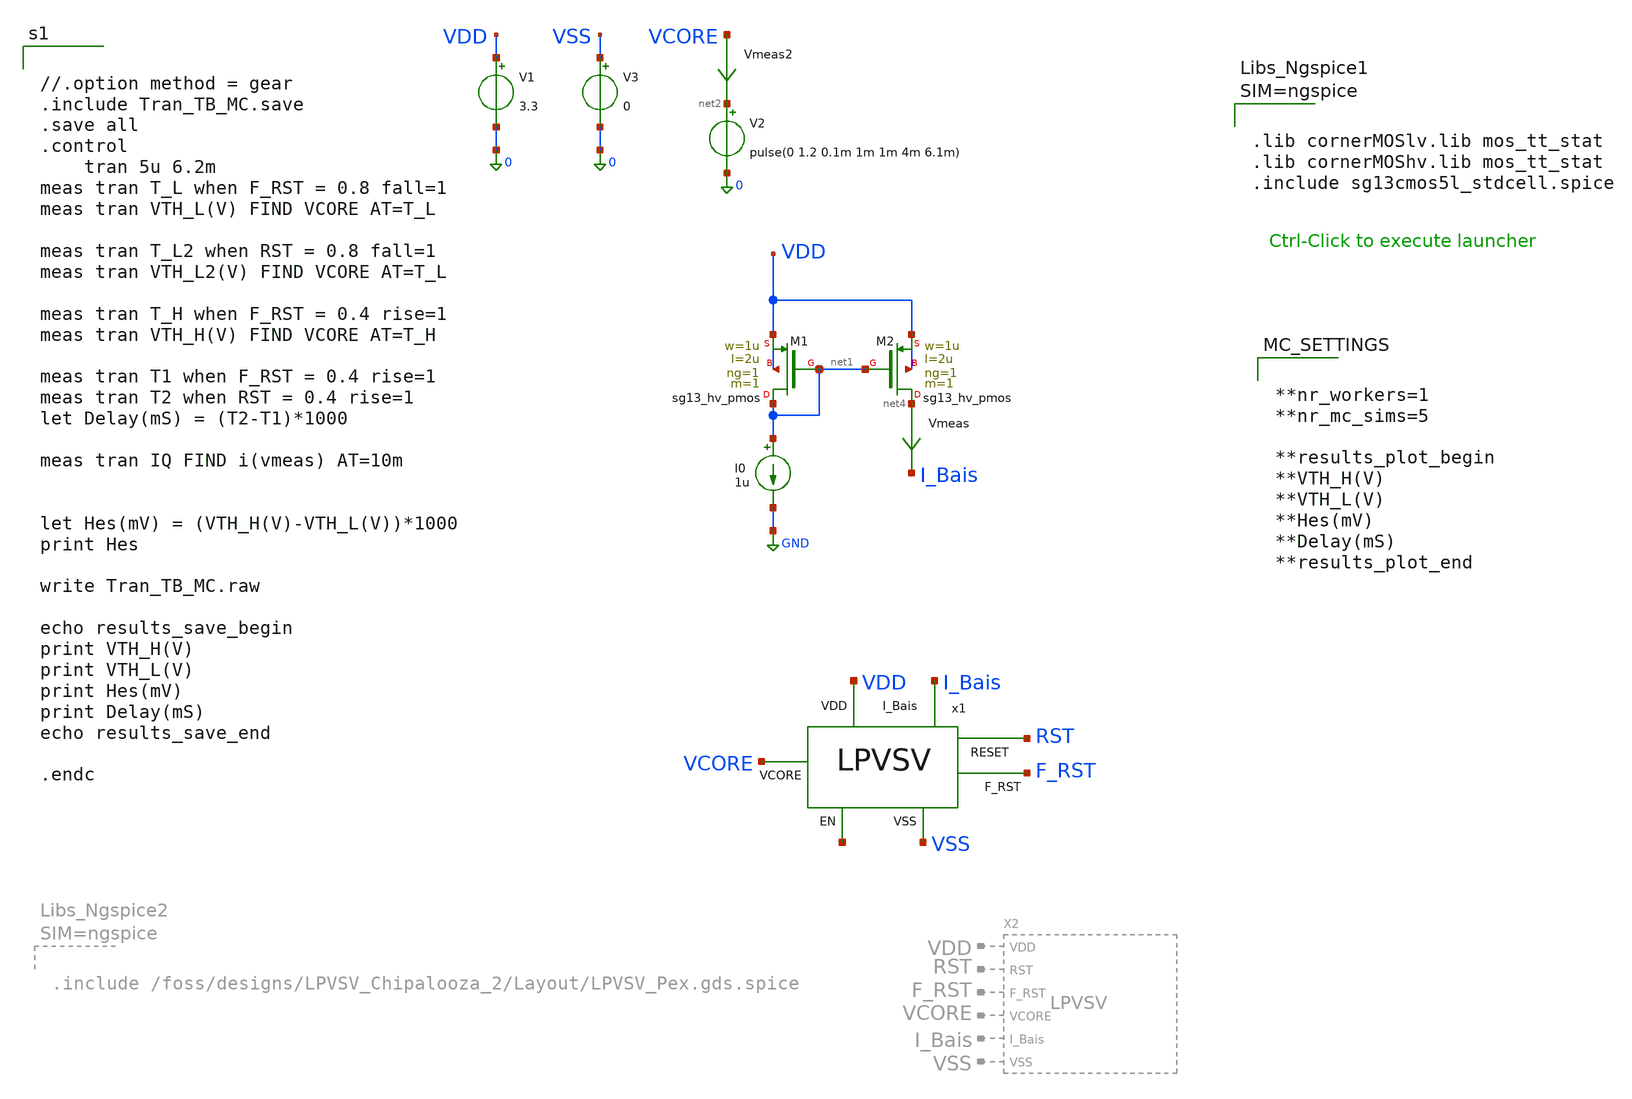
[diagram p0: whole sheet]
** sch_path: Simulation/Tran_TB_MC.sch
**.subckt Tran_TB_MC
V1 VDD 0 3.3
V2 net2 0 pulse(0 1.2 0.1m 1m 1m 4m 6.1m)
Vmeas2 VCORE net2 0
.save i(vmeas2)
V3 VSS 0 0
x1 VDD VCORE I_Bais RST F_RST VSS net3 LPVSV
I0 net1 GND 1u
Vmeas net4 I_Bais 0
.save i(vmeas)
XM1 net1 net1 VDD VDD sg13_hv_pmos w=1u l=2u ng=1 m=1 mm_ok=1
XM2 net4 net1 VDD VDD sg13_hv_pmos w=1u l=2u ng=1 m=1 mm_ok=1
**** begin user architecture code



.lib cornerMOSlv.lib mos_tt_stat
.lib cornerMOShv.lib mos_tt_stat
.include sg13cmos5l_stdcell.spice





**nr_workers=1
**nr_mc_sims=5

**results_plot_begin
**VTH_H(V)
**VTH_L(V)
**Hes(mV)
**Delay(mS)
**results_plot_end




//.option method = gear
.include Tran_TB_MC.save
.save all
.control
	tran 5u 6.2m
meas tran T_L when F_RST = 0.8 fall=1
meas tran VTH_L(V) FIND VCORE AT=T_L

meas tran T_L2 when RST = 0.8 fall=1
meas tran VTH_L2(V) FIND VCORE AT=T_L

meas tran T_H when F_RST = 0.4 rise=1
meas tran VTH_H(V) FIND VCORE AT=T_H

meas tran T1 when F_RST = 0.4 rise=1
meas tran T2 when RST = 0.4 rise=1
let Delay(mS) = (T2-T1)*1000

meas tran IQ FIND i(vmeas) AT=10m


let Hes(mV) = (VTH_H(V)-VTH_L(V))*1000
print Hes

write Tran_TB_MC.raw

echo results_save_begin
print VTH_H(V)
print VTH_L(V)
print Hes(mV)
print Delay(mS)
echo results_save_end

.endc


**** end user architecture code
**.ends
.GLOBAL GND
.end
